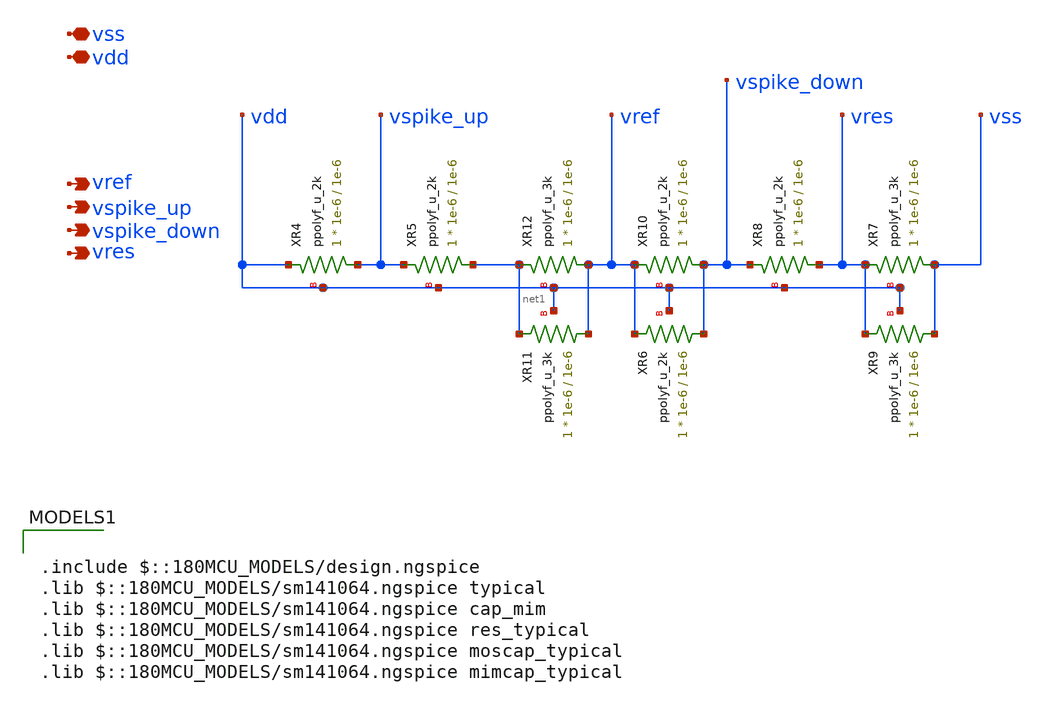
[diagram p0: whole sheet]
** sch_path: designs/libs/core_LIF_comp/core_vdiv/vdiv.sch
**.subckt vdiv vref vdd vss vspike_up vspike_down vres
*.opin vref
*.iopin vdd
*.iopin vss
*.opin vspike_up
*.opin vspike_down
*.opin vres
XR4 vspike_up vdd vdd ppolyf_u_2k r_width=1e-6 r_length=1e-6 m=1
XR5 net1 vspike_up vdd ppolyf_u_2k r_width=1e-6 r_length=1e-6 m=1
XR6 vspike_down vref vdd ppolyf_u_2k r_width=1e-6 r_length=1e-6 m=1
XR8 vres vspike_down vdd ppolyf_u_2k r_width=1e-6 r_length=1e-6 m=1
XR9 vss vres vdd ppolyf_u_3k r_width=1e-6 r_length=1e-6 m=1
XR7 vss vres vdd ppolyf_u_3k r_width=1e-6 r_length=1e-6 m=1
XR10 vspike_down vref vdd ppolyf_u_2k r_width=1e-6 r_length=1e-6 m=1
XR12 vref net1 vdd ppolyf_u_3k r_width=1e-6 r_length=1e-6 m=1
XR11 vref net1 vdd ppolyf_u_3k r_width=1e-6 r_length=1e-6 m=1
**** begin user architecture code

.include $::180MCU_MODELS/design.ngspice
.lib $::180MCU_MODELS/sm141064.ngspice typical
.lib $::180MCU_MODELS/sm141064.ngspice cap_mim
.lib $::180MCU_MODELS/sm141064.ngspice res_typical
.lib $::180MCU_MODELS/sm141064.ngspice moscap_typical
.lib $::180MCU_MODELS/sm141064.ngspice mimcap_typical

**** end user architecture code
**.ends
.end
